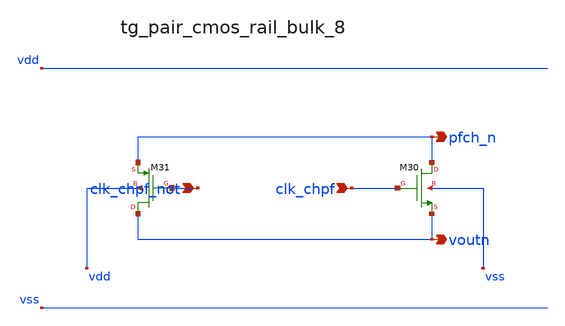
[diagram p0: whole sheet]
** sch_path: analog-db/raw/ia_003_fan_chopper_pf/hier/blocks/tg_pair_cmos_rail_bulk_8.sch
**.subckt tg_pair_cmos_rail_bulk_8 clk_chpf_not clk_chpf pfch_n voutn
*.ipin clk_chpf_not
*.ipin clk_chpf
*.opin pfch_n
*.opin voutn
XM30 pfch_n clk_chpf voutn vss sg13_lv_nmos w=x_dut_xm30_w l=x_dut_xm30_l ng=1 m=x_dut_xm30_m
XM31 voutn clk_chpf_not pfch_n vdd sg13_lv_pmos w=x_dut_xm31_w l=x_dut_xm31_l ng=1 m=x_dut_xm31_m
**.ends
.end
